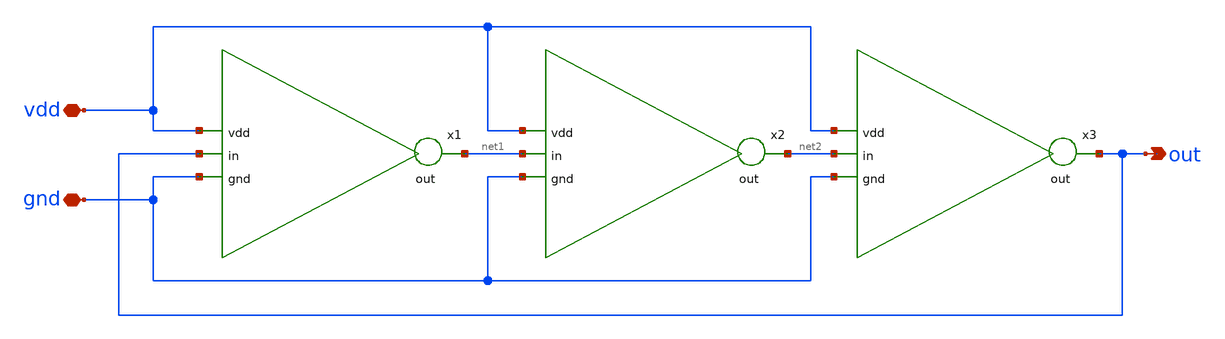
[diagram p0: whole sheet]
** sch_path: Inverter/ring_osc.sch
**.subckt ring_osc out vdd gnd
*.opin out
*.iopin vdd
*.iopin gnd
x1 vdd net1 out gnd inverter
x2 vdd net2 net1 gnd inverter
x3 vdd out net2 gnd inverter
**.ends
.end
